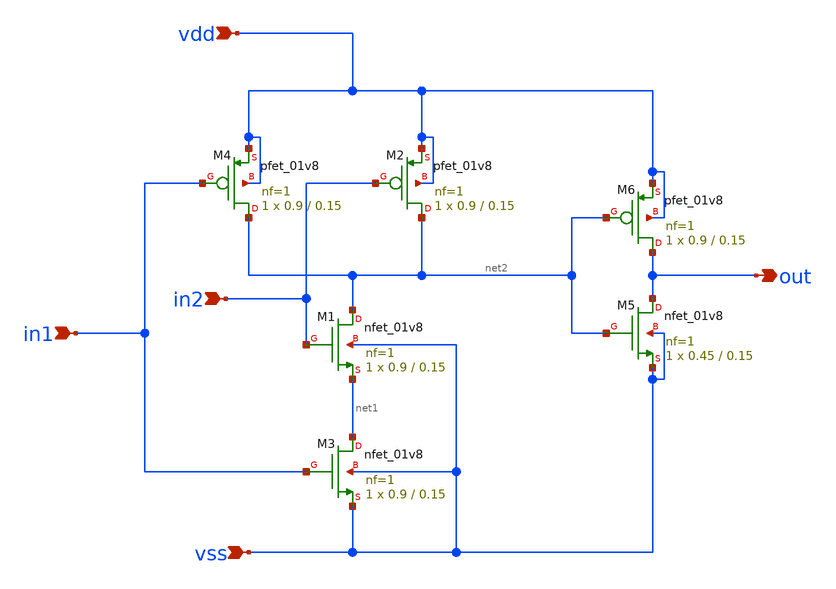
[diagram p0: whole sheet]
** sch_path: xschem/and_masa.sch
**.subckt and_masa out in2 vdd in1 vss
*.opin out
*.ipin in2
*.ipin vdd
*.ipin in1
*.ipin vss
XM1 net2 in2 net1 vss sky130_fd_pr__nfet_01v8 L=0.15 W=0.9 nf=1 ad='int((nf+1)/2) * W/nf * 0.29' as='int((nf+2)/2) * W/nf * 0.29'
+ pd='2*int((nf+1)/2) * (W/nf + 0.29)' ps='2*int((nf+2)/2) * (W/nf + 0.29)' nrd='0.29 / W' nrs='0.29 / W'
+ sa=0 sb=0 sd=0 mult=1 m=1
XM2 net2 in2 vdd vdd sky130_fd_pr__pfet_01v8 L=0.15 W=0.9 nf=1 ad='int((nf+1)/2) * W/nf * 0.29' as='int((nf+2)/2) * W/nf * 0.29'
+ pd='2*int((nf+1)/2) * (W/nf + 0.29)' ps='2*int((nf+2)/2) * (W/nf + 0.29)' nrd='0.29 / W' nrs='0.29 / W'
+ sa=0 sb=0 sd=0 mult=1 m=1
XM3 net1 in1 vss vss sky130_fd_pr__nfet_01v8 L=0.15 W=0.9 nf=1 ad='int((nf+1)/2) * W/nf * 0.29' as='int((nf+2)/2) * W/nf * 0.29'
+ pd='2*int((nf+1)/2) * (W/nf + 0.29)' ps='2*int((nf+2)/2) * (W/nf + 0.29)' nrd='0.29 / W' nrs='0.29 / W'
+ sa=0 sb=0 sd=0 mult=1 m=1
XM4 net2 in1 vdd vdd sky130_fd_pr__pfet_01v8 L=0.15 W=0.9 nf=1 ad='int((nf+1)/2) * W/nf * 0.29' as='int((nf+2)/2) * W/nf * 0.29'
+ pd='2*int((nf+1)/2) * (W/nf + 0.29)' ps='2*int((nf+2)/2) * (W/nf + 0.29)' nrd='0.29 / W' nrs='0.29 / W'
+ sa=0 sb=0 sd=0 mult=1 m=1
XM5 out net2 vss vss sky130_fd_pr__nfet_01v8 L=0.15 W=0.45 nf=1 ad='int((nf+1)/2) * W/nf * 0.29' as='int((nf+2)/2) * W/nf * 0.29'
+ pd='2*int((nf+1)/2) * (W/nf + 0.29)' ps='2*int((nf+2)/2) * (W/nf + 0.29)' nrd='0.29 / W' nrs='0.29 / W'
+ sa=0 sb=0 sd=0 mult=1 m=1
XM6 out net2 vdd vdd sky130_fd_pr__pfet_01v8 L=0.15 W=0.9 nf=1 ad='int((nf+1)/2) * W/nf * 0.29' as='int((nf+2)/2) * W/nf * 0.29'
+ pd='2*int((nf+1)/2) * (W/nf + 0.29)' ps='2*int((nf+2)/2) * (W/nf + 0.29)' nrd='0.29 / W' nrs='0.29 / W'
+ sa=0 sb=0 sd=0 mult=1 m=1
**.ends
.end
